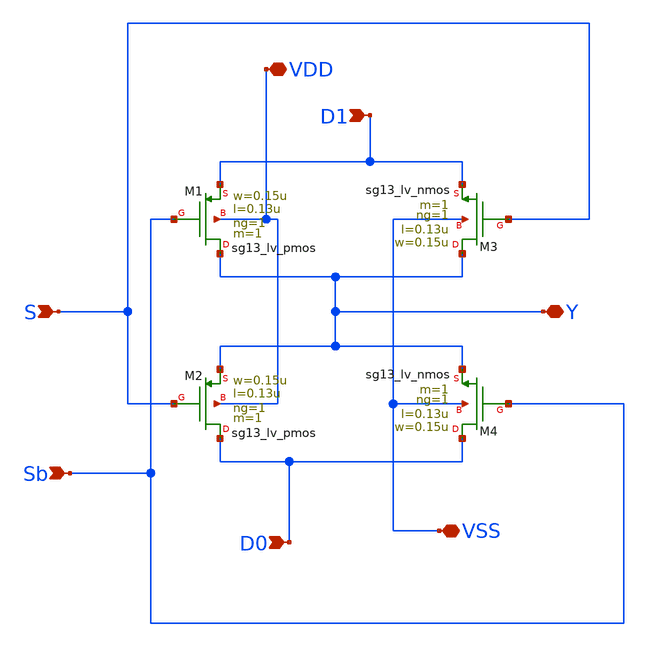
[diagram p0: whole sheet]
** sch_path: mux.sch
**.subckt mux S Sb D0 D1 VDD VSS Y
*.ipin S
*.ipin Sb
*.ipin D0
*.ipin D1
*.iopin VDD
*.iopin VSS
*.iopin Y
XM1 Y Sb D1 VDD sg13_lv_pmos w=0.15u l=0.13u ng=1 m=1 mm_ok=1
XM2 D0 S Y VDD sg13_lv_pmos w=0.15u l=0.13u ng=1 m=1 mm_ok=1
XM3 Y S D1 VSS sg13_lv_nmos w=0.15u l=0.13u ng=1 m=1 mm_ok=1
XM4 D0 Sb Y VSS sg13_lv_nmos w=0.15u l=0.13u ng=1 m=1 mm_ok=1
**.ends
.end
